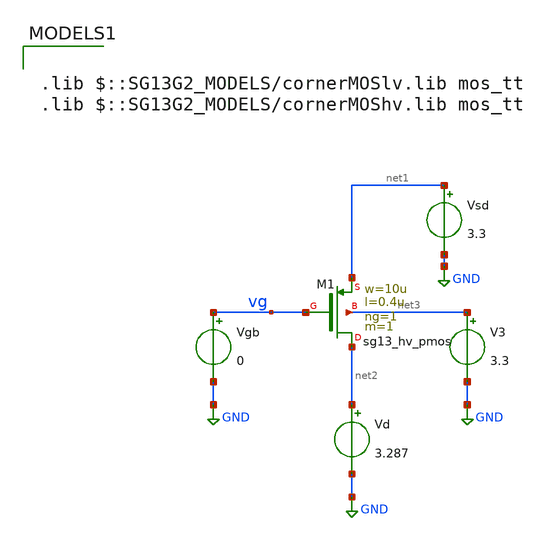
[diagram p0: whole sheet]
** sch_path: legacy/Examples/IHP-SG13/xschem/Extraction/pmos_ext.sch
**.subckt pmos_ext
Vgb vg GND 0
Vsd net1 GND 3.3
V3 net3 GND 3.3
Vd net2 GND 3.287
XM1 net2 vg net1 net3 sg13_hv_pmos w=10u l=0.4u ng=1 m=1 mm_ok=1
**** begin user architecture code



.control
pre_osdi ./psp103_nqs.osdi
save all
dc Vgb 0.05 3.05 10m

let gm_id = -deriv(ln(i(Vd)))
save gm_id

meas dc gm_id_max MAX gm_id
let gm_id_vt = 0.531*gm_id_max
save gm_id_vt

meas dc vt FIND V(vg) WHEN gm_id=gm_id_vt
let vt0=vt-3.3
meas dc is0_ FIND i(Vd) WHEN V(vg)=vt

let is0 = is0_/0.88
let VT_val=0.026
let n = 1/(gm_id_max*VT_val)
save is0 vt0 n
echo
echo
echo

echo Extracted parameters:
print is0 vt0 n


echo
echo
echo

remzerovec
write pmos_ext.raw

.endc




.lib $::SG13G2_MODELS/cornerMOSlv.lib mos_tt
.lib $::SG13G2_MODELS/cornerMOShv.lib mos_tt

**** end user architecture code
**.ends
.GLOBAL GND
.end
